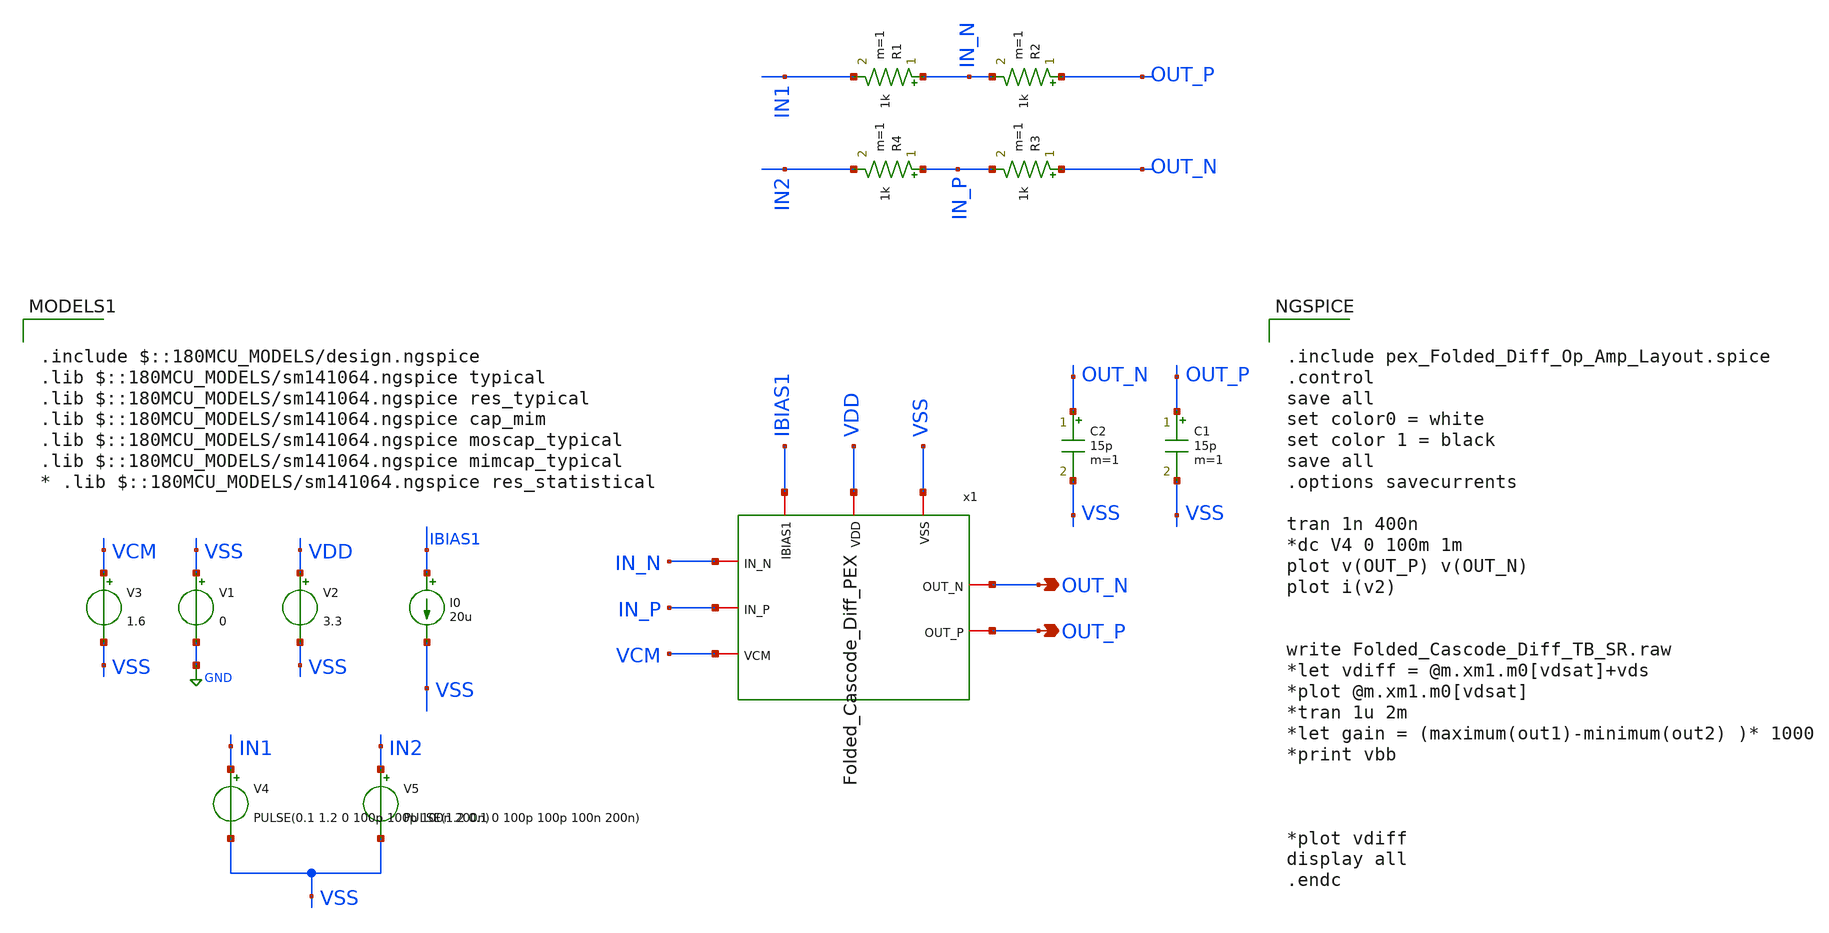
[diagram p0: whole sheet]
** sch_path: SCOP_INPUT_AND_MUX_PAKISTAN_03/Xschem/Folded_Cascode_Amplifier/Folded_Cascode_Diff_TB_SR.sch
**.subckt Folded_Cascode_Diff_TB_SR OUT_N OUT_P
*.opin OUT_N
*.opin OUT_P
V1 VSS GND 0
V2 VDD VSS 3.3
V3 VCM VSS 1.6
I0 IBIAS1 VSS 20u
V5 IN2 VSS PULSE(1.2 0.1 0 100p 100p 100n 200n)
C1 OUT_P VSS 15p m=1
C2 OUT_N VSS 15p m=1
R1 IN_N IN1 1k m=1
R2 OUT_P IN_N 1k m=1
R3 OUT_N IN_P 1k m=1
R4 IN_P IN2 1k m=1
V4 IN1 VSS PULSE(0.1 1.2 0 100p 100p 100n 200n)
x1 VDD VSS IN_N IN_P IBIAS1 VCM OUT_N OUT_P Folded_Cascode_Diff_PEX
**** begin user architecture code


.include pex_Folded_Diff_Op_Amp_Layout.spice
.control
save all
set color0 = white
set color 1 = black
save all
.options savecurrents

tran 1n 400n
*dc V4 0 100m 1m
plot v(OUT_P) v(OUT_N)
plot i(v2)


write Folded_Cascode_Diff_TB_SR.raw
*let vdiff = @m.xm1.m0[vdsat]+vds
*plot @m.xm1.m0[vdsat]
*tran 1u 2m
*let gain = (maximum(out1)-minimum(out2) )* 1000
*print vbb



*plot vdiff
display all
.endc



.include $::180MCU_MODELS/design.ngspice
.lib $::180MCU_MODELS/sm141064.ngspice typical
.lib $::180MCU_MODELS/sm141064.ngspice res_typical
.lib $::180MCU_MODELS/sm141064.ngspice cap_mim
.lib $::180MCU_MODELS/sm141064.ngspice moscap_typical
.lib $::180MCU_MODELS/sm141064.ngspice mimcap_typical
* .lib $::180MCU_MODELS/sm141064.ngspice res_statistical

**** end user architecture code
**.ends
.GLOBAL GND
.end
